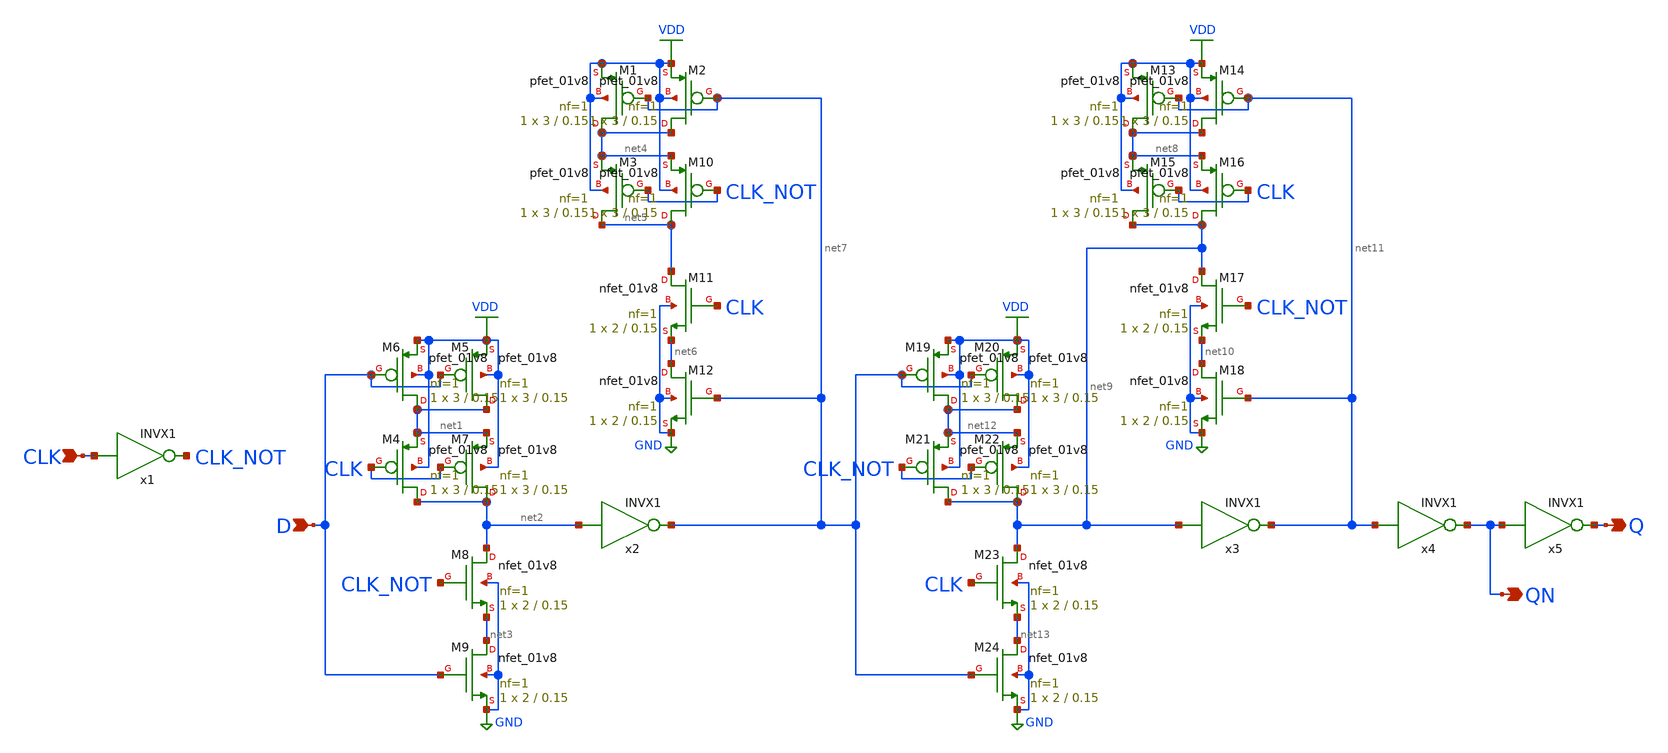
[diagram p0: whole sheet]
** sch_path: lib/xschem/DFF.sch
**.subckt DFF CLK QN Q D
*.ipin CLK
*.opin QN
*.opin Q
*.ipin D
x1 CLK_NOT CLK INVX1
x2 net7 net2 INVX1
x3 net11 net9 INVX1
x4 QN net11 INVX1
x5 Q QN INVX1
XM8 net2 CLK_NOT net3 GND sky130_fd_pr__nfet_01v8 L=0.15 W=2 nf=1 ad='int((nf+1)/2) * W/nf * 0.29' as='int((nf+2)/2) * W/nf * 0.29'
+ pd='2*int((nf+1)/2) * (W/nf + 0.29)' ps='2*int((nf+2)/2) * (W/nf + 0.29)' nrd='0.29 / W' nrs='0.29 / W'
+ sa=0 sb=0 sd=0 mult=1 m=1
XM6 net1 D VDD VDD sky130_fd_pr__pfet_01v8 L=0.15 W=3 nf=1 ad='int((nf+1)/2) * W/nf * 0.29' as='int((nf+2)/2) * W/nf * 0.29'
+ pd='2*int((nf+1)/2) * (W/nf + 0.29)' ps='2*int((nf+2)/2) * (W/nf + 0.29)' nrd='0.29 / W' nrs='0.29 / W'
+ sa=0 sb=0 sd=0 mult=1 m=1
XM9 net3 D GND GND sky130_fd_pr__nfet_01v8 L=0.15 W=2 nf=1 ad='int((nf+1)/2) * W/nf * 0.29' as='int((nf+2)/2) * W/nf * 0.29'
+ pd='2*int((nf+1)/2) * (W/nf + 0.29)' ps='2*int((nf+2)/2) * (W/nf + 0.29)' nrd='0.29 / W' nrs='0.29 / W'
+ sa=0 sb=0 sd=0 mult=1 m=1
XM4 net2 CLK net1 VDD sky130_fd_pr__pfet_01v8 L=0.15 W=3 nf=1 ad='int((nf+1)/2) * W/nf * 0.29' as='int((nf+2)/2) * W/nf * 0.29'
+ pd='2*int((nf+1)/2) * (W/nf + 0.29)' ps='2*int((nf+2)/2) * (W/nf + 0.29)' nrd='0.29 / W' nrs='0.29 / W'
+ sa=0 sb=0 sd=0 mult=1 m=1
XM5 net1 D VDD VDD sky130_fd_pr__pfet_01v8 L=0.15 W=3 nf=1 ad='int((nf+1)/2) * W/nf * 0.29' as='int((nf+2)/2) * W/nf * 0.29'
+ pd='2*int((nf+1)/2) * (W/nf + 0.29)' ps='2*int((nf+2)/2) * (W/nf + 0.29)' nrd='0.29 / W' nrs='0.29 / W'
+ sa=0 sb=0 sd=0 mult=1 m=1
XM7 net2 CLK net1 VDD sky130_fd_pr__pfet_01v8 L=0.15 W=3 nf=1 ad='int((nf+1)/2) * W/nf * 0.29' as='int((nf+2)/2) * W/nf * 0.29'
+ pd='2*int((nf+1)/2) * (W/nf + 0.29)' ps='2*int((nf+2)/2) * (W/nf + 0.29)' nrd='0.29 / W' nrs='0.29 / W'
+ sa=0 sb=0 sd=0 mult=1 m=1
XM11 net5 CLK net6 GND sky130_fd_pr__nfet_01v8 L=0.15 W=2 nf=1 ad='int((nf+1)/2) * W/nf * 0.29' as='int((nf+2)/2) * W/nf * 0.29'
+ pd='2*int((nf+1)/2) * (W/nf + 0.29)' ps='2*int((nf+2)/2) * (W/nf + 0.29)' nrd='0.29 / W' nrs='0.29 / W'
+ sa=0 sb=0 sd=0 mult=1 m=1
XM12 net6 net7 GND GND sky130_fd_pr__nfet_01v8 L=0.15 W=2 nf=1 ad='int((nf+1)/2) * W/nf * 0.29' as='int((nf+2)/2) * W/nf * 0.29'
+ pd='2*int((nf+1)/2) * (W/nf + 0.29)' ps='2*int((nf+2)/2) * (W/nf + 0.29)' nrd='0.29 / W' nrs='0.29 / W'
+ sa=0 sb=0 sd=0 mult=1 m=1
XM1 net4 net7 VDD VDD sky130_fd_pr__pfet_01v8 L=0.15 W=3 nf=1 ad='int((nf+1)/2) * W/nf * 0.29' as='int((nf+2)/2) * W/nf * 0.29'
+ pd='2*int((nf+1)/2) * (W/nf + 0.29)' ps='2*int((nf+2)/2) * (W/nf + 0.29)' nrd='0.29 / W' nrs='0.29 / W'
+ sa=0 sb=0 sd=0 mult=1 m=1
XM2 net4 net7 VDD VDD sky130_fd_pr__pfet_01v8 L=0.15 W=3 nf=1 ad='int((nf+1)/2) * W/nf * 0.29' as='int((nf+2)/2) * W/nf * 0.29'
+ pd='2*int((nf+1)/2) * (W/nf + 0.29)' ps='2*int((nf+2)/2) * (W/nf + 0.29)' nrd='0.29 / W' nrs='0.29 / W'
+ sa=0 sb=0 sd=0 mult=1 m=1
XM3 net5 CLK_NOT net4 VDD sky130_fd_pr__pfet_01v8 L=0.15 W=3 nf=1 ad='int((nf+1)/2) * W/nf * 0.29' as='int((nf+2)/2) * W/nf * 0.29'
+ pd='2*int((nf+1)/2) * (W/nf + 0.29)' ps='2*int((nf+2)/2) * (W/nf + 0.29)' nrd='0.29 / W' nrs='0.29 / W'
+ sa=0 sb=0 sd=0 mult=1 m=1
XM10 net5 CLK_NOT net4 VDD sky130_fd_pr__pfet_01v8 L=0.15 W=3 nf=1 ad='int((nf+1)/2) * W/nf * 0.29' as='int((nf+2)/2) * W/nf * 0.29'
+ pd='2*int((nf+1)/2) * (W/nf + 0.29)' ps='2*int((nf+2)/2) * (W/nf + 0.29)' nrd='0.29 / W' nrs='0.29 / W'
+ sa=0 sb=0 sd=0 mult=1 m=1
XM19 net12 net7 VDD VDD sky130_fd_pr__pfet_01v8 L=0.15 W=3 nf=1 ad='int((nf+1)/2) * W/nf * 0.29' as='int((nf+2)/2) * W/nf * 0.29'
+ pd='2*int((nf+1)/2) * (W/nf + 0.29)' ps='2*int((nf+2)/2) * (W/nf + 0.29)' nrd='0.29 / W' nrs='0.29 / W'
+ sa=0 sb=0 sd=0 mult=1 m=1
XM20 net12 net7 VDD VDD sky130_fd_pr__pfet_01v8 L=0.15 W=3 nf=1 ad='int((nf+1)/2) * W/nf * 0.29' as='int((nf+2)/2) * W/nf * 0.29'
+ pd='2*int((nf+1)/2) * (W/nf + 0.29)' ps='2*int((nf+2)/2) * (W/nf + 0.29)' nrd='0.29 / W' nrs='0.29 / W'
+ sa=0 sb=0 sd=0 mult=1 m=1
XM21 net9 CLK_NOT net12 VDD sky130_fd_pr__pfet_01v8 L=0.15 W=3 nf=1 ad='int((nf+1)/2) * W/nf * 0.29'
+ as='int((nf+2)/2) * W/nf * 0.29' pd='2*int((nf+1)/2) * (W/nf + 0.29)' ps='2*int((nf+2)/2) * (W/nf + 0.29)'
+ nrd='0.29 / W' nrs='0.29 / W' sa=0 sb=0 sd=0 mult=1 m=1
XM22 net9 CLK_NOT net12 VDD sky130_fd_pr__pfet_01v8 L=0.15 W=3 nf=1 ad='int((nf+1)/2) * W/nf * 0.29'
+ as='int((nf+2)/2) * W/nf * 0.29' pd='2*int((nf+1)/2) * (W/nf + 0.29)' ps='2*int((nf+2)/2) * (W/nf + 0.29)'
+ nrd='0.29 / W' nrs='0.29 / W' sa=0 sb=0 sd=0 mult=1 m=1
XM23 net9 CLK net13 GND sky130_fd_pr__nfet_01v8 L=0.15 W=2 nf=1 ad='int((nf+1)/2) * W/nf * 0.29' as='int((nf+2)/2) * W/nf * 0.29'
+ pd='2*int((nf+1)/2) * (W/nf + 0.29)' ps='2*int((nf+2)/2) * (W/nf + 0.29)' nrd='0.29 / W' nrs='0.29 / W'
+ sa=0 sb=0 sd=0 mult=1 m=1
XM24 net13 net7 GND GND sky130_fd_pr__nfet_01v8 L=0.15 W=2 nf=1 ad='int((nf+1)/2) * W/nf * 0.29' as='int((nf+2)/2) * W/nf * 0.29'
+ pd='2*int((nf+1)/2) * (W/nf + 0.29)' ps='2*int((nf+2)/2) * (W/nf + 0.29)' nrd='0.29 / W' nrs='0.29 / W'
+ sa=0 sb=0 sd=0 mult=1 m=1
XM13 net8 net11 VDD VDD sky130_fd_pr__pfet_01v8 L=0.15 W=3 nf=1 ad='int((nf+1)/2) * W/nf * 0.29' as='int((nf+2)/2) * W/nf * 0.29'
+ pd='2*int((nf+1)/2) * (W/nf + 0.29)' ps='2*int((nf+2)/2) * (W/nf + 0.29)' nrd='0.29 / W' nrs='0.29 / W'
+ sa=0 sb=0 sd=0 mult=1 m=1
XM14 net8 net11 VDD VDD sky130_fd_pr__pfet_01v8 L=0.15 W=3 nf=1 ad='int((nf+1)/2) * W/nf * 0.29' as='int((nf+2)/2) * W/nf * 0.29'
+ pd='2*int((nf+1)/2) * (W/nf + 0.29)' ps='2*int((nf+2)/2) * (W/nf + 0.29)' nrd='0.29 / W' nrs='0.29 / W'
+ sa=0 sb=0 sd=0 mult=1 m=1
XM15 net9 CLK net8 VDD sky130_fd_pr__pfet_01v8 L=0.15 W=3 nf=1 ad='int((nf+1)/2) * W/nf * 0.29' as='int((nf+2)/2) * W/nf * 0.29'
+ pd='2*int((nf+1)/2) * (W/nf + 0.29)' ps='2*int((nf+2)/2) * (W/nf + 0.29)' nrd='0.29 / W' nrs='0.29 / W'
+ sa=0 sb=0 sd=0 mult=1 m=1
XM16 net9 CLK net8 VDD sky130_fd_pr__pfet_01v8 L=0.15 W=3 nf=1 ad='int((nf+1)/2) * W/nf * 0.29' as='int((nf+2)/2) * W/nf * 0.29'
+ pd='2*int((nf+1)/2) * (W/nf + 0.29)' ps='2*int((nf+2)/2) * (W/nf + 0.29)' nrd='0.29 / W' nrs='0.29 / W'
+ sa=0 sb=0 sd=0 mult=1 m=1
XM17 net9 CLK_NOT net10 GND sky130_fd_pr__nfet_01v8 L=0.15 W=2 nf=1 ad='int((nf+1)/2) * W/nf * 0.29'
+ as='int((nf+2)/2) * W/nf * 0.29' pd='2*int((nf+1)/2) * (W/nf + 0.29)' ps='2*int((nf+2)/2) * (W/nf + 0.29)'
+ nrd='0.29 / W' nrs='0.29 / W' sa=0 sb=0 sd=0 mult=1 m=1
XM18 net10 net11 GND GND sky130_fd_pr__nfet_01v8 L=0.15 W=2 nf=1 ad='int((nf+1)/2) * W/nf * 0.29' as='int((nf+2)/2) * W/nf * 0.29'
+ pd='2*int((nf+1)/2) * (W/nf + 0.29)' ps='2*int((nf+2)/2) * (W/nf + 0.29)' nrd='0.29 / W' nrs='0.29 / W'
+ sa=0 sb=0 sd=0 mult=1 m=1
**.ends
.GLOBAL GND
.GLOBAL VDD
.end
